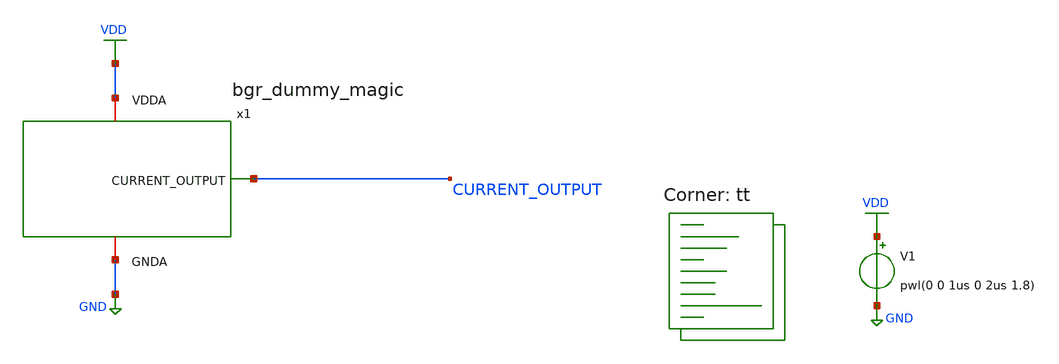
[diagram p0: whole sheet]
** sch_path: projects/pll/full_pll/xschem_ngspice/tb_cur_gen_dummy_magic.sch
**.subckt tb_cur_gen_dummy_magic
V1 VDD GND pwl(0 0 1us 0 2us 1.8)
x1 VDD CURRENT_OUTPUT GND bgr_dummy_magic
**** begin user architecture code
.lib $::SKYWATER_MODELS/sky130.lib.spice tt



* ngspice commands

.include /foss/designs/my_design/projects/pll/full_pll/xschem_ngspice/bgr_dummy_magic.spice

.option method=gear
.option wnflag=1
* .option savecurrents
* .temp =140

.save @m.x1.x0.msky130_fd_pr__pfet_01v8[id] @m.x1.x17.msky130_fd_pr__pfet_01v8[id] @m.x1.x26.msky130_fd_pr__pfet_01v8[id] @m.x1.x35.msky130_fd_pr__pfet_01v8[id] @m.x1.x44.msky130_fd_pr__pfet_01v8[id] @m.x1.x95.msky130_fd_pr__pfet_01v8[id] @m.x1.x109.msky130_fd_pr__pfet_01v8[id] @m.x1.x117.msky130_fd_pr__pfet_01v8[id] @m.x1.x127.msky130_fd_pr__pfet_01v8[id] @m.x1.x160.msky130_fd_pr__pfet_01v8[id] @m.xm1.msky130_fd_pr__pfet_01v8[gm] @m.xm1.msky130_fd_pr__pfet_01v8[vth] @m.xm1.msky130_fd_pr__pfet_01v8[vgs] @m.xm1.msky130_fd_pr__pfet_01v8[vds] @m.x1.xm1.msky130_fd_pr__nfet_01v8[gm]

* .ic v(vin-) = 0.8
* .ic v(vin+) = 0.8
* .ic v(v_top) = 1.8

.control

    save all
    * dc temp -40 120 5 V1 1.6 2.0 0.05
    * dc V1 1.7 1.9 0.001 temp -40 120 40
    * dc V1 0.0 2.0 0.02 temp -40 120 20
    * dc V1 0 2.0 0.02
    tran 0.4ns 5us
    remzerovec
    write tb_cur_gen_dummy_magic.raw
.endc




**** end user architecture code
**.ends
.GLOBAL GND
.GLOBAL VDD
.end
